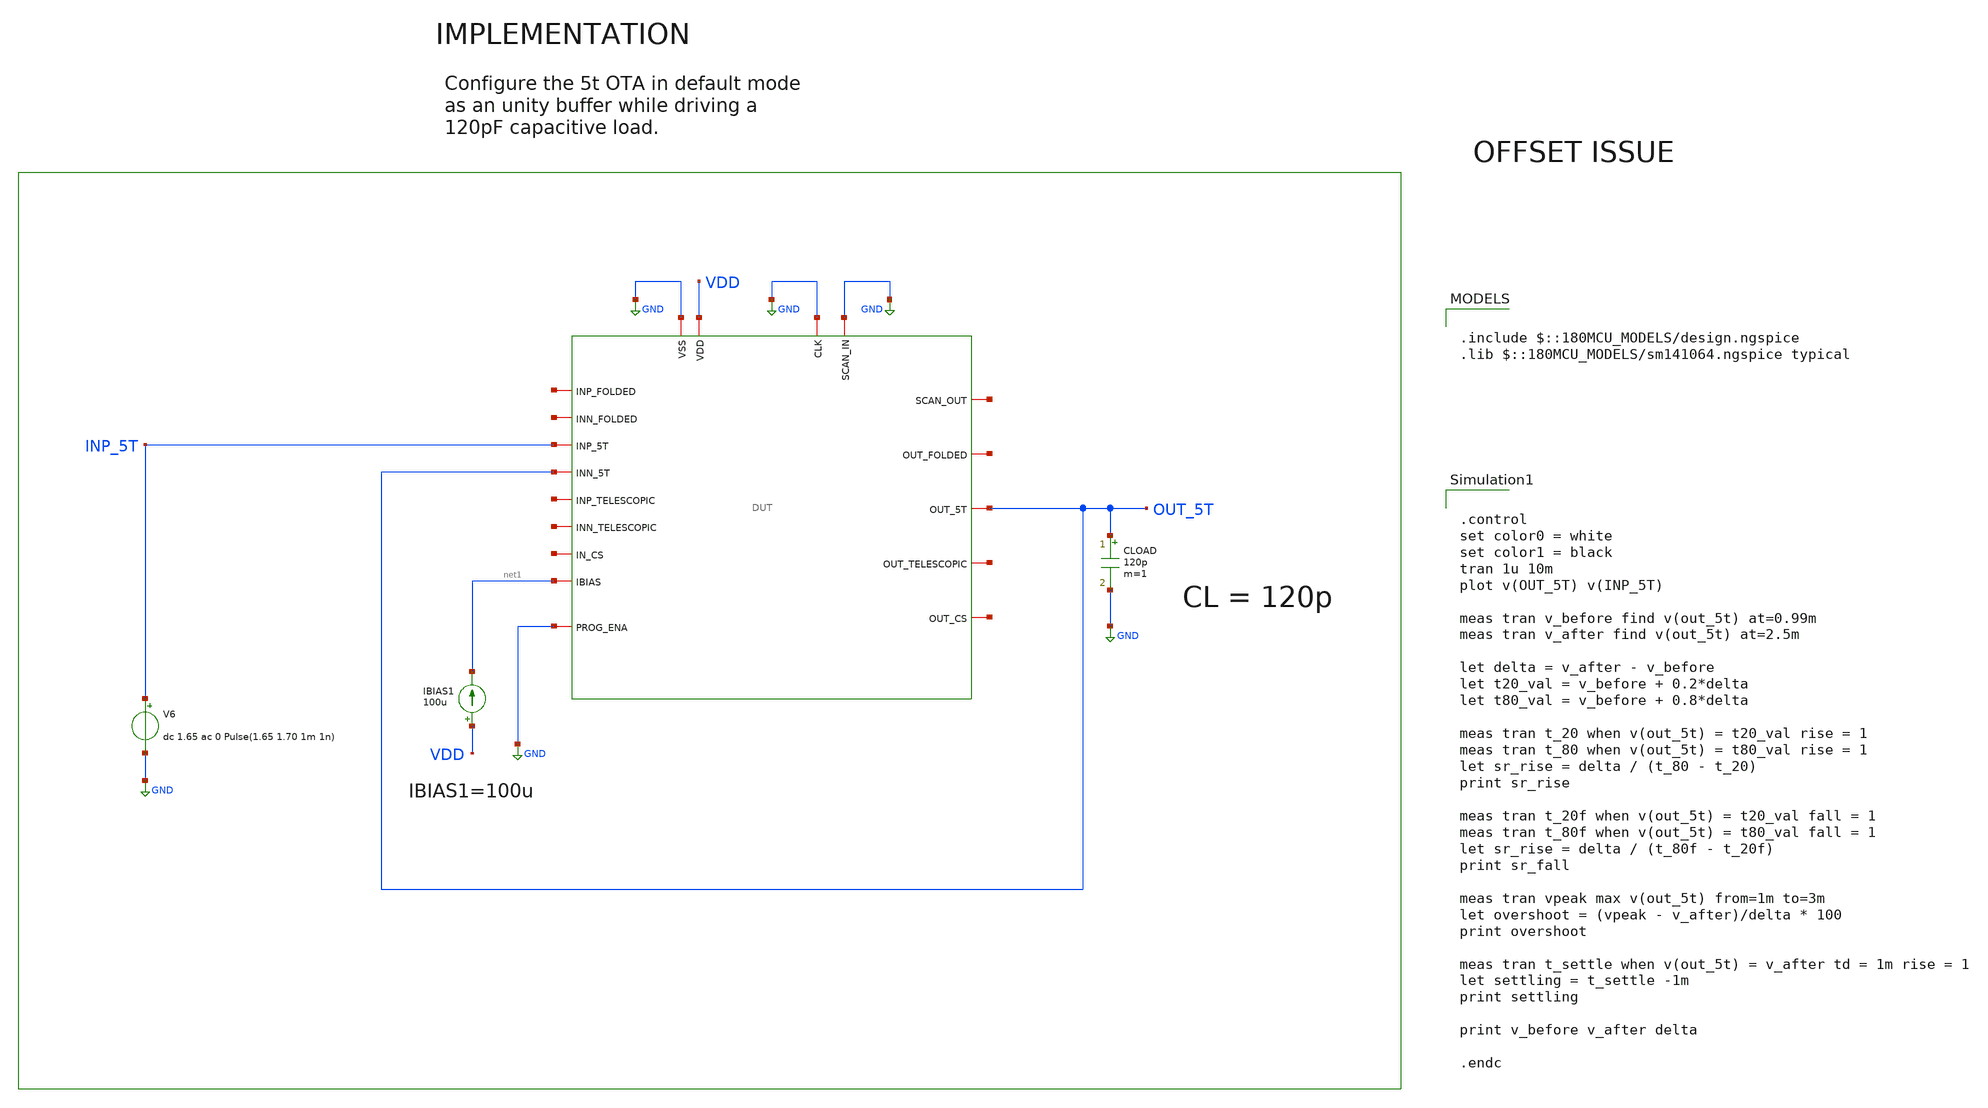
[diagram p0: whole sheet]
** sch_path: designs/libs/verification/ota_5t/defult_sizing/5t_unity_step_tb.sch
**.subckt 5t_unity_step_tb
IBIAS1 VDD net1 100u
CLOAD OUT_5T GND 120p m=1
V6 INP_5T GND dc 1.65 ac 0 Pulse(1.65 1.70 1m 1n)
x1 GND net2 GND GND VDD net3 net4 OUT_5T net1 net5 INP_5T OUT_5T net6 net7 net8 net9 net10 GND DUT
**** begin user architecture code

.include $::180MCU_MODELS/design.ngspice
.lib $::180MCU_MODELS/sm141064.ngspice typical



.control
set color0 = white
set color1 = black
tran 1u 10m
plot v(OUT_5T) v(INP_5T)

meas tran v_before find v(out_5t) at=0.99m
meas tran v_after find v(out_5t) at=2.5m

let delta = v_after - v_before
let t20_val = v_before + 0.2*delta
let t80_val = v_before + 0.8*delta

meas tran t_20 when v(out_5t) = t20_val rise = 1
meas tran t_80 when v(out_5t) = t80_val rise = 1
let sr_rise = delta / (t_80 - t_20)
print sr_rise

meas tran t_20f when v(out_5t) = t20_val fall = 1
meas tran t_80f when v(out_5t) = t80_val fall = 1
let sr_rise = delta / (t_80f - t_20f)
print sr_fall

meas tran vpeak max v(out_5t) from=1m to=3m
let overshoot = (vpeak - v_after)/delta * 100
print overshoot

meas tran t_settle when v(out_5t) = v_after td = 1m rise = 1
let settling = t_settle -1m
print settling

print v_before v_after delta

.endc


**** end user architecture code
**.ends
.GLOBAL GND
.end
